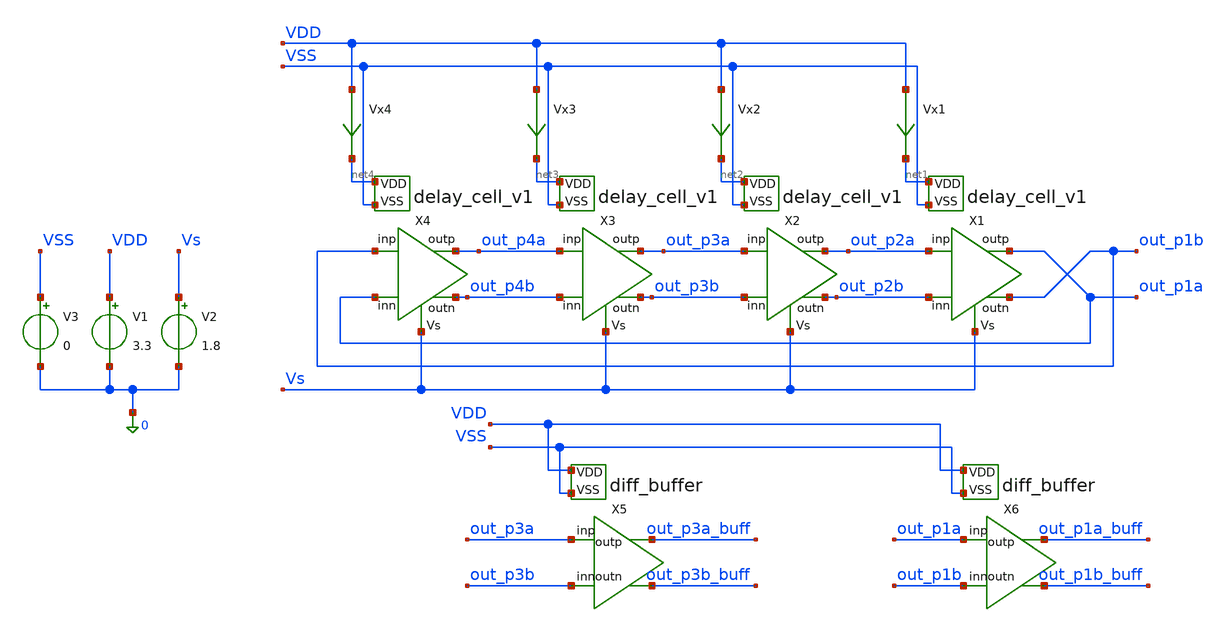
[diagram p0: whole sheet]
** sch_path: xschem/delay_cell_tb.sch
**.subckt delay_cell_tb
V1 VDD 0 3.3
.save i(v1)
V2 Vs 0 1.8
.save i(v2)
V3 VSS 0 0
.save i(v3)
Vx1 VDD net1 0
.save i(vx1)
Vx2 VDD net2 0
.save i(vx2)
X1 net1 out_p1b out_p1a out_p2a out_p2b Vs VSS delay_cell_v1
X2 net2 out_p2b out_p2a out_p3a out_p3b Vs VSS delay_cell_v1
X5 VDD out_p3b_buff out_p3a_buff out_p3a out_p3b VSS diff_buffer
Vx3 VDD net3 0
.save i(vx3)
X3 net3 out_p3b out_p3a out_p4a out_p4b Vs VSS delay_cell_v1
Vx4 VDD net4 0
.save i(vx4)
X4 net4 out_p4b out_p4a out_p1b out_p1a Vs VSS delay_cell_v1
X6 VDD out_p1b_buff out_p1a_buff out_p1a out_p1b VSS diff_buffer
**** begin user architecture code


.include delay_cell_tb.save
.option savecurrents method=gear
.save all
.control
  tran 0.01n 10n
  remzerovec
  write delay_cell_tb.raw
.endc



.include $::180MCU_MODELS/design.ngspice
.lib $::180MCU_MODELS/sm141064.ngspice typical

**** end user architecture code
**.ends

* expanding   symbol:  xschem/delay_cell_v1.sym # of pins=7
** sym_path: xschem/delay_cell_v1.sym
** sch_path: xschem/delay_cell_v1.sch
.subckt delay_cell_v1 VDD outn outp inp inn Vs VSS
*.ipin inp
*.ipin inn
*.opin outp
*.opin outn
*.ipin VDD
*.ipin VSS
*.ipin Vs
XM_DUT outn outn VDD VDD pfet_03v3 L=0.28u W=2.0u nf=1 ad='int((nf+1)/2) * W/nf * 0.18u' as='int((nf+2)/2) * W/nf * 0.18u'
+ pd='2*int((nf+1)/2) * (W/nf + 0.18u)' ps='2*int((nf+2)/2) * (W/nf + 0.18u)' nrd='0.18u / W' nrs='0.18u / W'
+ sa=0 sb=0 sd=0 m=1 par=1
XM1 vtail Vs VSS VSS nfet_03v3 L=0.28u W=16u nf=8 ad='int((nf+1)/2) * W/nf * 0.18u' as='int((nf+2)/2) * W/nf * 0.18u'
+ pd='2*int((nf+1)/2) * (W/nf + 0.18u)' ps='2*int((nf+2)/2) * (W/nf + 0.18u)' nrd='0.18u / W' nrs='0.18u / W'
+ sa=0 sb=0 sd=0 m=1 par=1
XM_DUT2 outn outp VDD VDD pfet_03v3 L=0.28u W=4.0u nf=2 ad='int((nf+1)/2) * W/nf * 0.18u' as='int((nf+2)/2) * W/nf * 0.18u'
+ pd='2*int((nf+1)/2) * (W/nf + 0.18u)' ps='2*int((nf+2)/2) * (W/nf + 0.18u)' nrd='0.18u / W' nrs='0.18u / W'
+ sa=0 sb=0 sd=0 m=1 par=1
XM3 outp inn vtail VSS nfet_03v3 L=0.28u W=3u nf=1 ad='int((nf+1)/2) * W/nf * 0.18u' as='int((nf+2)/2) * W/nf * 0.18u'
+ pd='2*int((nf+1)/2) * (W/nf + 0.18u)' ps='2*int((nf+2)/2) * (W/nf + 0.18u)' nrd='0.18u / W' nrs='0.18u / W'
+ sa=0 sb=0 sd=0 m=1 par=1
XM2 outn inp vtail VSS nfet_03v3 L=0.28u W=3u nf=1 ad='int((nf+1)/2) * W/nf * 0.18u' as='int((nf+2)/2) * W/nf * 0.18u'
+ pd='2*int((nf+1)/2) * (W/nf + 0.18u)' ps='2*int((nf+2)/2) * (W/nf + 0.18u)' nrd='0.18u / W' nrs='0.18u / W'
+ sa=0 sb=0 sd=0 m=1 par=1
XM_DUT5 outp outp VDD VDD pfet_03v3 L=0.28u W=2.0u nf=1 ad='int((nf+1)/2) * W/nf * 0.18u' as='int((nf+2)/2) * W/nf * 0.18u'
+ pd='2*int((nf+1)/2) * (W/nf + 0.18u)' ps='2*int((nf+2)/2) * (W/nf + 0.18u)' nrd='0.18u / W' nrs='0.18u / W'
+ sa=0 sb=0 sd=0 m=1 par=1
XM_DUT6 outp outn VDD VDD pfet_03v3 L=0.28u W=4.0u nf=2 ad='int((nf+1)/2) * W/nf * 0.18u' as='int((nf+2)/2) * W/nf * 0.18u'
+ pd='2*int((nf+1)/2) * (W/nf + 0.18u)' ps='2*int((nf+2)/2) * (W/nf + 0.18u)' nrd='0.18u / W' nrs='0.18u / W'
+ sa=0 sb=0 sd=0 m=1 par=1
.ends


* expanding   symbol:  xschem/diff_buffer.sym # of pins=6
** sym_path: xschem/diff_buffer.sym
** sch_path: xschem/diff_buffer.sch
.subckt diff_buffer VDD outn outp inp inn VSS
*.ipin inn
*.opin outp
*.opin outn
*.ipin VDD
*.ipin VSS
*.ipin inp
XM_DUT1 net1 inn VDD VDD pfet_03v3 L=0.28u W=4.0u nf=2 ad='int((nf+1)/2) * W/nf * 0.18u' as='int((nf+2)/2) * W/nf * 0.18u'
+ pd='2*int((nf+1)/2) * (W/nf + 0.18u)' ps='2*int((nf+2)/2) * (W/nf + 0.18u)' nrd='0.18u / W' nrs='0.18u / W'
+ sa=0 sb=0 sd=0 m=1 par=1
XM1 net1 inn VSS VSS nfet_03v3 L=0.28u W=2u nf=1 ad='int((nf+1)/2) * W/nf * 0.18u' as='int((nf+2)/2) * W/nf * 0.18u'
+ pd='2*int((nf+1)/2) * (W/nf + 0.18u)' ps='2*int((nf+2)/2) * (W/nf + 0.18u)' nrd='0.18u / W' nrs='0.18u / W'
+ sa=0 sb=0 sd=0 m=1 par=1
XM_DUT2 net2 inp VDD VDD pfet_03v3 L=0.28u W=4.0u nf=2 ad='int((nf+1)/2) * W/nf * 0.18u' as='int((nf+2)/2) * W/nf * 0.18u'
+ pd='2*int((nf+1)/2) * (W/nf + 0.18u)' ps='2*int((nf+2)/2) * (W/nf + 0.18u)' nrd='0.18u / W' nrs='0.18u / W'
+ sa=0 sb=0 sd=0 m=1 par=1
XM2 net2 inp VSS VSS nfet_03v3 L=0.28u W=2u nf=1 ad='int((nf+1)/2) * W/nf * 0.18u' as='int((nf+2)/2) * W/nf * 0.18u'
+ pd='2*int((nf+1)/2) * (W/nf + 0.18u)' ps='2*int((nf+2)/2) * (W/nf + 0.18u)' nrd='0.18u / W' nrs='0.18u / W'
+ sa=0 sb=0 sd=0 m=1 par=1
XM_DUT3 net3 net1 VDD VDD pfet_03v3 L=0.28u W=4.0u nf=2 ad='int((nf+1)/2) * W/nf * 0.18u' as='int((nf+2)/2) * W/nf * 0.18u'
+ pd='2*int((nf+1)/2) * (W/nf + 0.18u)' ps='2*int((nf+2)/2) * (W/nf + 0.18u)' nrd='0.18u / W' nrs='0.18u / W'
+ sa=0 sb=0 sd=0 m=1 par=1
XM3 net3 net1 VSS VSS nfet_03v3 L=0.28u W=2u nf=1 ad='int((nf+1)/2) * W/nf * 0.18u' as='int((nf+2)/2) * W/nf * 0.18u'
+ pd='2*int((nf+1)/2) * (W/nf + 0.18u)' ps='2*int((nf+2)/2) * (W/nf + 0.18u)' nrd='0.18u / W' nrs='0.18u / W'
+ sa=0 sb=0 sd=0 m=1 par=1
XM_DUT4 net4 net2 VDD VDD pfet_03v3 L=0.28u W=4.0u nf=2 ad='int((nf+1)/2) * W/nf * 0.18u' as='int((nf+2)/2) * W/nf * 0.18u'
+ pd='2*int((nf+1)/2) * (W/nf + 0.18u)' ps='2*int((nf+2)/2) * (W/nf + 0.18u)' nrd='0.18u / W' nrs='0.18u / W'
+ sa=0 sb=0 sd=0 m=1 par=1
XM4 net4 net2 VSS VSS nfet_03v3 L=0.28u W=2u nf=1 ad='int((nf+1)/2) * W/nf * 0.18u' as='int((nf+2)/2) * W/nf * 0.18u'
+ pd='2*int((nf+1)/2) * (W/nf + 0.18u)' ps='2*int((nf+2)/2) * (W/nf + 0.18u)' nrd='0.18u / W' nrs='0.18u / W'
+ sa=0 sb=0 sd=0 m=1 par=1
XM_DUT5 net3 net4 VDD VDD pfet_03v3 L=0.28u W=4.0u nf=2 ad='int((nf+1)/2) * W/nf * 0.18u' as='int((nf+2)/2) * W/nf * 0.18u'
+ pd='2*int((nf+1)/2) * (W/nf + 0.18u)' ps='2*int((nf+2)/2) * (W/nf + 0.18u)' nrd='0.18u / W' nrs='0.18u / W'
+ sa=0 sb=0 sd=0 m=1 par=1
XM5 net3 net4 VSS VSS nfet_03v3 L=0.28u W=2u nf=1 ad='int((nf+1)/2) * W/nf * 0.18u' as='int((nf+2)/2) * W/nf * 0.18u'
+ pd='2*int((nf+1)/2) * (W/nf + 0.18u)' ps='2*int((nf+2)/2) * (W/nf + 0.18u)' nrd='0.18u / W' nrs='0.18u / W'
+ sa=0 sb=0 sd=0 m=1 par=1
XM_DUT6 net4 net3 VDD VDD pfet_03v3 L=0.28u W=4.0u nf=2 ad='int((nf+1)/2) * W/nf * 0.18u' as='int((nf+2)/2) * W/nf * 0.18u'
+ pd='2*int((nf+1)/2) * (W/nf + 0.18u)' ps='2*int((nf+2)/2) * (W/nf + 0.18u)' nrd='0.18u / W' nrs='0.18u / W'
+ sa=0 sb=0 sd=0 m=1 par=1
XM6 net4 net3 VSS VSS nfet_03v3 L=0.28u W=2u nf=1 ad='int((nf+1)/2) * W/nf * 0.18u' as='int((nf+2)/2) * W/nf * 0.18u'
+ pd='2*int((nf+1)/2) * (W/nf + 0.18u)' ps='2*int((nf+2)/2) * (W/nf + 0.18u)' nrd='0.18u / W' nrs='0.18u / W'
+ sa=0 sb=0 sd=0 m=1 par=1
XM_DUT7 net5 net3 VDD VDD pfet_03v3 L=0.28u W=4.0u nf=2 ad='int((nf+1)/2) * W/nf * 0.18u' as='int((nf+2)/2) * W/nf * 0.18u'
+ pd='2*int((nf+1)/2) * (W/nf + 0.18u)' ps='2*int((nf+2)/2) * (W/nf + 0.18u)' nrd='0.18u / W' nrs='0.18u / W'
+ sa=0 sb=0 sd=0 m=1 par=1
XM7 net5 net3 VSS VSS nfet_03v3 L=0.28u W=2u nf=1 ad='int((nf+1)/2) * W/nf * 0.18u' as='int((nf+2)/2) * W/nf * 0.18u'
+ pd='2*int((nf+1)/2) * (W/nf + 0.18u)' ps='2*int((nf+2)/2) * (W/nf + 0.18u)' nrd='0.18u / W' nrs='0.18u / W'
+ sa=0 sb=0 sd=0 m=1 par=1
XM_DUT8 net6 net4 VDD VDD pfet_03v3 L=0.28u W=4.0u nf=2 ad='int((nf+1)/2) * W/nf * 0.18u' as='int((nf+2)/2) * W/nf * 0.18u'
+ pd='2*int((nf+1)/2) * (W/nf + 0.18u)' ps='2*int((nf+2)/2) * (W/nf + 0.18u)' nrd='0.18u / W' nrs='0.18u / W'
+ sa=0 sb=0 sd=0 m=1 par=1
XM8 net6 net4 VSS VSS nfet_03v3 L=0.28u W=2u nf=1 ad='int((nf+1)/2) * W/nf * 0.18u' as='int((nf+2)/2) * W/nf * 0.18u'
+ pd='2*int((nf+1)/2) * (W/nf + 0.18u)' ps='2*int((nf+2)/2) * (W/nf + 0.18u)' nrd='0.18u / W' nrs='0.18u / W'
+ sa=0 sb=0 sd=0 m=1 par=1
XM_DUT9 outn net5 VDD VDD pfet_03v3 L=0.28u W=4.0u nf=2 ad='int((nf+1)/2) * W/nf * 0.18u' as='int((nf+2)/2) * W/nf * 0.18u'
+ pd='2*int((nf+1)/2) * (W/nf + 0.18u)' ps='2*int((nf+2)/2) * (W/nf + 0.18u)' nrd='0.18u / W' nrs='0.18u / W'
+ sa=0 sb=0 sd=0 m=1 par=1
XM9 outn net5 VSS VSS nfet_03v3 L=0.28u W=2u nf=1 ad='int((nf+1)/2) * W/nf * 0.18u' as='int((nf+2)/2) * W/nf * 0.18u'
+ pd='2*int((nf+1)/2) * (W/nf + 0.18u)' ps='2*int((nf+2)/2) * (W/nf + 0.18u)' nrd='0.18u / W' nrs='0.18u / W'
+ sa=0 sb=0 sd=0 m=1 par=1
XM_DUT10 outp net6 VDD VDD pfet_03v3 L=0.28u W=4.0u nf=2 ad='int((nf+1)/2) * W/nf * 0.18u' as='int((nf+2)/2) * W/nf * 0.18u'
+ pd='2*int((nf+1)/2) * (W/nf + 0.18u)' ps='2*int((nf+2)/2) * (W/nf + 0.18u)' nrd='0.18u / W' nrs='0.18u / W'
+ sa=0 sb=0 sd=0 m=1 par=1
XM10 outp net6 VSS VSS nfet_03v3 L=0.28u W=2u nf=1 ad='int((nf+1)/2) * W/nf * 0.18u' as='int((nf+2)/2) * W/nf * 0.18u'
+ pd='2*int((nf+1)/2) * (W/nf + 0.18u)' ps='2*int((nf+2)/2) * (W/nf + 0.18u)' nrd='0.18u / W' nrs='0.18u / W'
+ sa=0 sb=0 sd=0 m=1 par=1
.ends

.end
